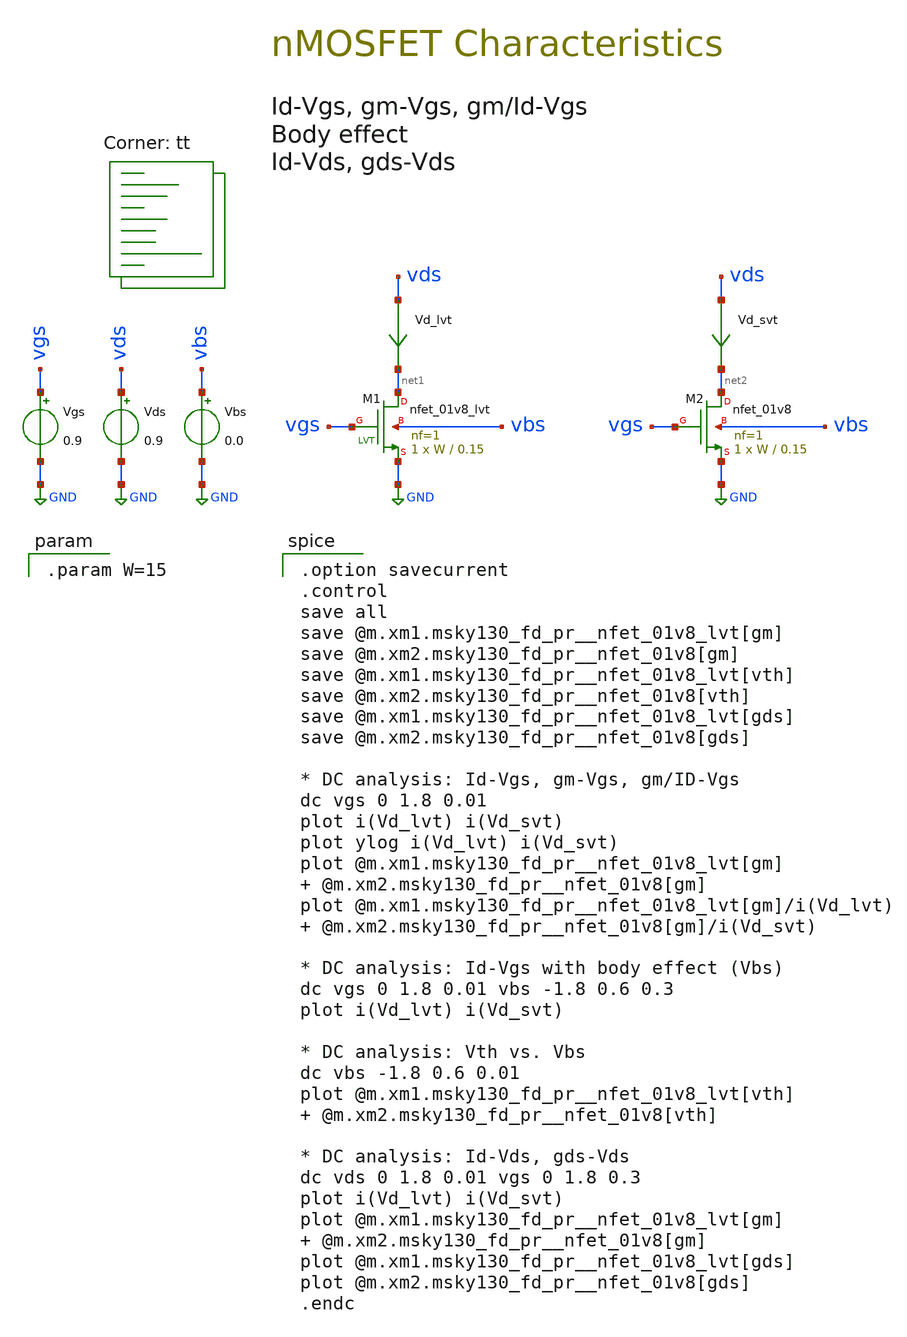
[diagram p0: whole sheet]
** sch_path: 00-a_nfet.sch
**.subckt 00-a_nfet
XM1 net1 vgs GND vbs sky130_fd_pr__nfet_01v8_lvt L=0.15 W=W nf=1 ad='int((1 + 1)/2) * W / 1 * 0.29' as='int((1 + 2)/2) * W / 1 * 0.29'
+ pd='2*int((1 + 1)/2) * (W / 1 + 0.29)' ps='2*int((1 + 2)/2) * (W / 1 + 0.29)' nrd='0.29 / W ' nrs='0.29 / W '
+ sa=0 sb=0 sd=0 mult=1 m=1
Vgs vgs GND 0.9
Vds vds GND 0.9
Vd_lvt vds net1 0
.save i(vd_lvt)
Vbs vbs GND 0.0
XM2 net2 vgs GND vbs sky130_fd_pr__nfet_01v8 L=0.15 W=W nf=1 ad='int((1 + 1)/2) * W / 1 * 0.29' as='int((1 + 2)/2) * W / 1 * 0.29'
+ pd='2*int((1 + 1)/2) * (W / 1 + 0.29)' ps='2*int((1 + 2)/2) * (W / 1 + 0.29)' nrd='0.29 / W ' nrs='0.29 / W '
+ sa=0 sb=0 sd=0 mult=1 m=1
Vd_svt vds net2 0
.save i(vd_svt)
**** begin user architecture code

.option savecurrent
.control
save all
save @m.xm1.msky130_fd_pr__nfet_01v8_lvt[gm]
save @m.xm2.msky130_fd_pr__nfet_01v8[gm]
save @m.xm1.msky130_fd_pr__nfet_01v8_lvt[vth]
save @m.xm2.msky130_fd_pr__nfet_01v8[vth]
save @m.xm1.msky130_fd_pr__nfet_01v8_lvt[gds]
save @m.xm2.msky130_fd_pr__nfet_01v8[gds]

* DC analysis: Id-Vgs, gm-Vgs, gm/ID-Vgs
dc vgs 0 1.8 0.01
plot i(Vd_lvt) i(Vd_svt)
plot ylog i(Vd_lvt) i(Vd_svt)
plot @m.xm1.msky130_fd_pr__nfet_01v8_lvt[gm]  @m.xm2.msky130_fd_pr__nfet_01v8[gm]
plot @m.xm1.msky130_fd_pr__nfet_01v8_lvt[gm]/i(Vd_lvt)
+  @m.xm2.msky130_fd_pr__nfet_01v8[gm]/i(Vd_svt)

* DC analysis: Id-Vgs with body effect (Vbs)
dc vgs 0 1.8 0.01 vbs -1.8 0.6 0.3
plot i(Vd_lvt) i(Vd_svt)

* DC analysis: Vth vs. Vbs
dc vbs -1.8 0.6 0.01
plot @m.xm1.msky130_fd_pr__nfet_01v8_lvt[vth]  @m.xm2.msky130_fd_pr__nfet_01v8[vth]

* DC analysis: Id-Vds, gds-Vds
dc vds 0 1.8 0.01 vgs 0 1.8 0.3
plot i(Vd_lvt) i(Vd_svt)
plot @m.xm1.msky130_fd_pr__nfet_01v8_lvt[gm]  @m.xm2.msky130_fd_pr__nfet_01v8[gm]
plot @m.xm1.msky130_fd_pr__nfet_01v8_lvt[gds]
plot @m.xm2.msky130_fd_pr__nfet_01v8[gds]
.endc

.lib $::SKYWATER_MODELS/sky130.lib.spice tt

.param W=15

**** end user architecture code
**.ends
.GLOBAL GND
.end
